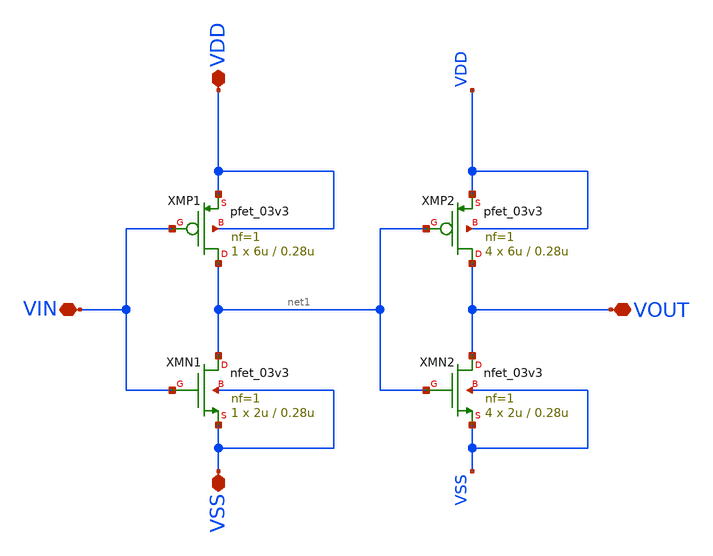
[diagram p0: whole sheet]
** sch_path: designs/sar_adc/digital/gate_buf_input/xschem/gate_buf_input.sch
**.subckt gate_buf_input VDD VSS VIN VOUT
*.iopin VDD
*.iopin VSS
*.iopin VIN
*.iopin VOUT
XMN1 net1 VIN VSS VSS nfet_03v3 L=0.28u W=2u nf=1 ad='int((nf+1)/2) * W/nf * 0.18u' as='int((nf+2)/2) * W/nf * 0.18u'
+ pd='2*int((nf+1)/2) * (W/nf + 0.18u)' ps='2*int((nf+2)/2) * (W/nf + 0.18u)' nrd='0.18u / W' nrs='0.18u / W'
+ sa=0 sb=0 sd=0 m=1
XMP1 net1 VIN VDD VDD pfet_03v3 L=0.28u W=6u nf=1 ad='int((nf+1)/2) * W/nf * 0.18u' as='int((nf+2)/2) * W/nf * 0.18u'
+ pd='2*int((nf+1)/2) * (W/nf + 0.18u)' ps='2*int((nf+2)/2) * (W/nf + 0.18u)' nrd='0.18u / W' nrs='0.18u / W'
+ sa=0 sb=0 sd=0 m=1
XMP2 VOUT net1 VDD VDD pfet_03v3 L=0.28u W=6u nf=1 ad='int((nf+1)/2) * W/nf * 0.18u' as='int((nf+2)/2) * W/nf * 0.18u'
+ pd='2*int((nf+1)/2) * (W/nf + 0.18u)' ps='2*int((nf+2)/2) * (W/nf + 0.18u)' nrd='0.18u / W' nrs='0.18u / W'
+ sa=0 sb=0 sd=0 m=4
XMN2 VOUT net1 VSS VSS nfet_03v3 L=0.28u W=2u nf=1 ad='int((nf+1)/2) * W/nf * 0.18u' as='int((nf+2)/2) * W/nf * 0.18u'
+ pd='2*int((nf+1)/2) * (W/nf + 0.18u)' ps='2*int((nf+2)/2) * (W/nf + 0.18u)' nrd='0.18u / W' nrs='0.18u / W'
+ sa=0 sb=0 sd=0 m=4
**.ends
.end
